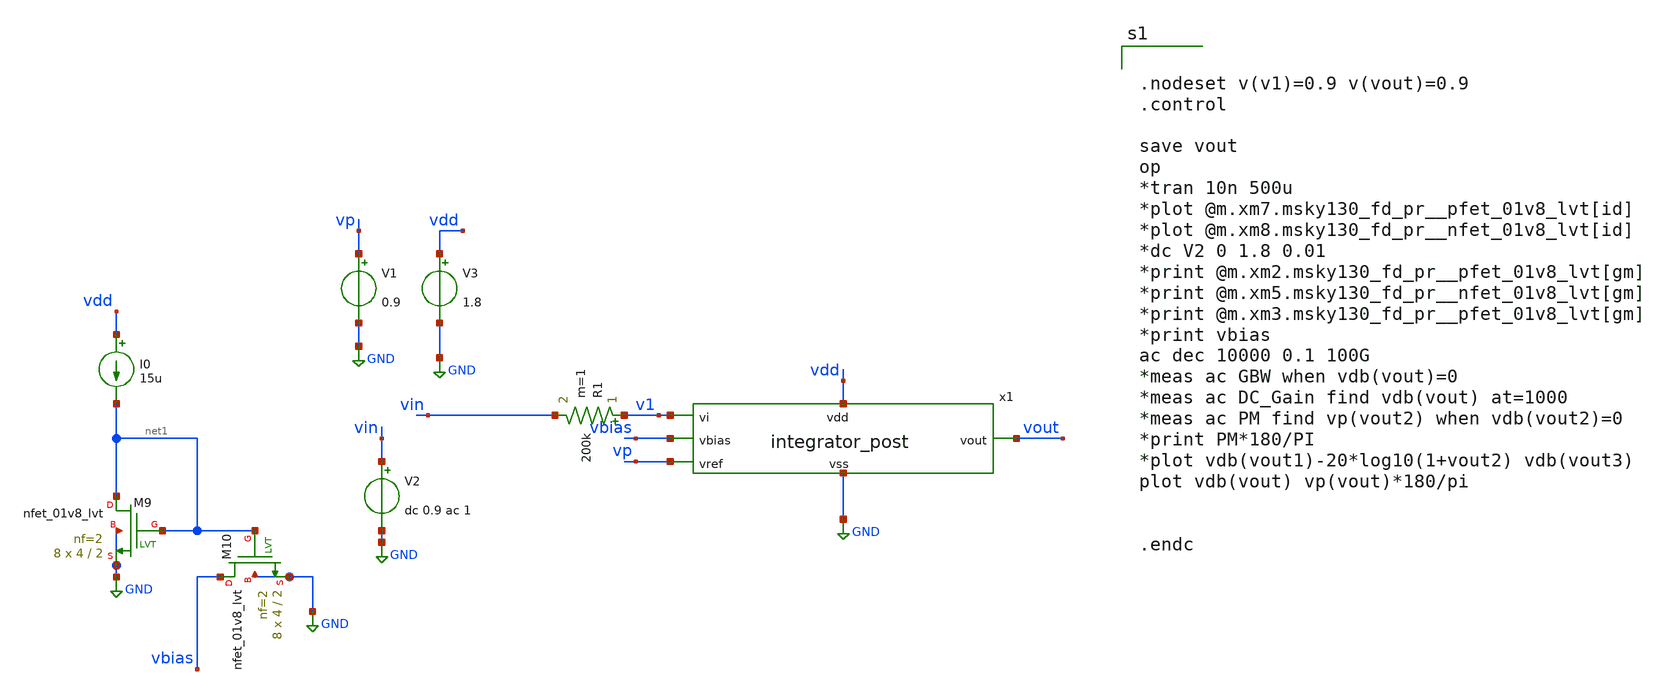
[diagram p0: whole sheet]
** sch_path: xschem/src/integrator/integrator_tb.sch
**.subckt integrator_tb
I0 vdd net1 15u
V1 vp GND 0.9
V3 vdd GND 1.8
XM9 net1 net1 GND GND sky130_fd_pr__nfet_01v8_lvt L=2 W=4 nf=2 ad='int((nf+1)/2) * W/nf * 0.29' as='int((nf+2)/2) * W/nf * 0.29'
+ pd='2*int((nf+1)/2) * (W/nf + 0.29)' ps='2*int((nf+2)/2) * (W/nf + 0.29)' nrd='0.29 / W' nrs='0.29 / W'
+ sa=0 sb=0 sd=0 mult=8 m=8
XM10 vbias net1 GND GND sky130_fd_pr__nfet_01v8_lvt L=2 W=4 nf=2 ad='int((nf+1)/2) * W/nf * 0.29' as='int((nf+2)/2) * W/nf * 0.29'
+ pd='2*int((nf+1)/2) * (W/nf + 0.29)' ps='2*int((nf+2)/2) * (W/nf + 0.29)' nrd='0.29 / W' nrs='0.29 / W'
+ sa=0 sb=0 sd=0 mult=8 m=8
V2 vin GND dc 0.9 ac 1
x1 vdd v1 vbias vp GND vout integrator_post
R1 v1 vin 200k m=1
**** begin user architecture code


.nodeset v(v1)=0.9 v(vout)=0.9
.control

save vout
op
*tran 10n 500u
*plot @m.xm7.msky130_fd_pr__pfet_01v8_lvt[id]
*plot @m.xm8.msky130_fd_pr__nfet_01v8_lvt[id]
*dc V2 0 1.8 0.01
*print @m.xm2.msky130_fd_pr__pfet_01v8_lvt[gm]
*print @m.xm5.msky130_fd_pr__nfet_01v8_lvt[gm]
*print @m.xm3.msky130_fd_pr__pfet_01v8_lvt[gm]
*print vbias
ac dec 10000 0.1 100G
*meas ac GBW when vdb(vout)=0
*meas ac DC_Gain find vdb(vout) at=1000
*meas ac PM find vp(vout2) when vdb(vout2)=0
*print PM*180/PI
*plot vdb(vout1)-20*log10(1+vout2) vdb(vout3)
plot vdb(vout) vp(vout)*180/pi


.endc



.include /home/eda/pdk/skywater-pdk/libraries/sky130_fd_pr_ngspice/latest/models/corners/tt.spice
.include /home/eda/magic/class_d_audio_amplifier/OTA/OTA_post.spice
.include /home/eda/magic/class_d_audio_amplifier/OTA/OTA_tri_post.spice
.include /home/eda/magic/class_d_audio_amplifier/OTA/OTA_int_post.spice
.include /home/eda/magic/class_d_audio_amplifier/OTA/OTA_int_revised_post.spice
.include /home/eda/magic/class_d_audio_amplifier/integrator/integrator_post.spice
* Resistor$::SKYWATER_MODELS/Capacitor
.include $::SKYWATER_MODELS/models/r+c/res_typical__cap_typical.spice
.include $::SKYWATER_MODELS/models/r+c/res_typical__cap_typical__lin.spice
* Special cells
.include $::SKYWATER_MODELS/models/corners/tt/specialized_cells.spice


**** end user architecture code
**.ends
.GLOBAL GND
.end
